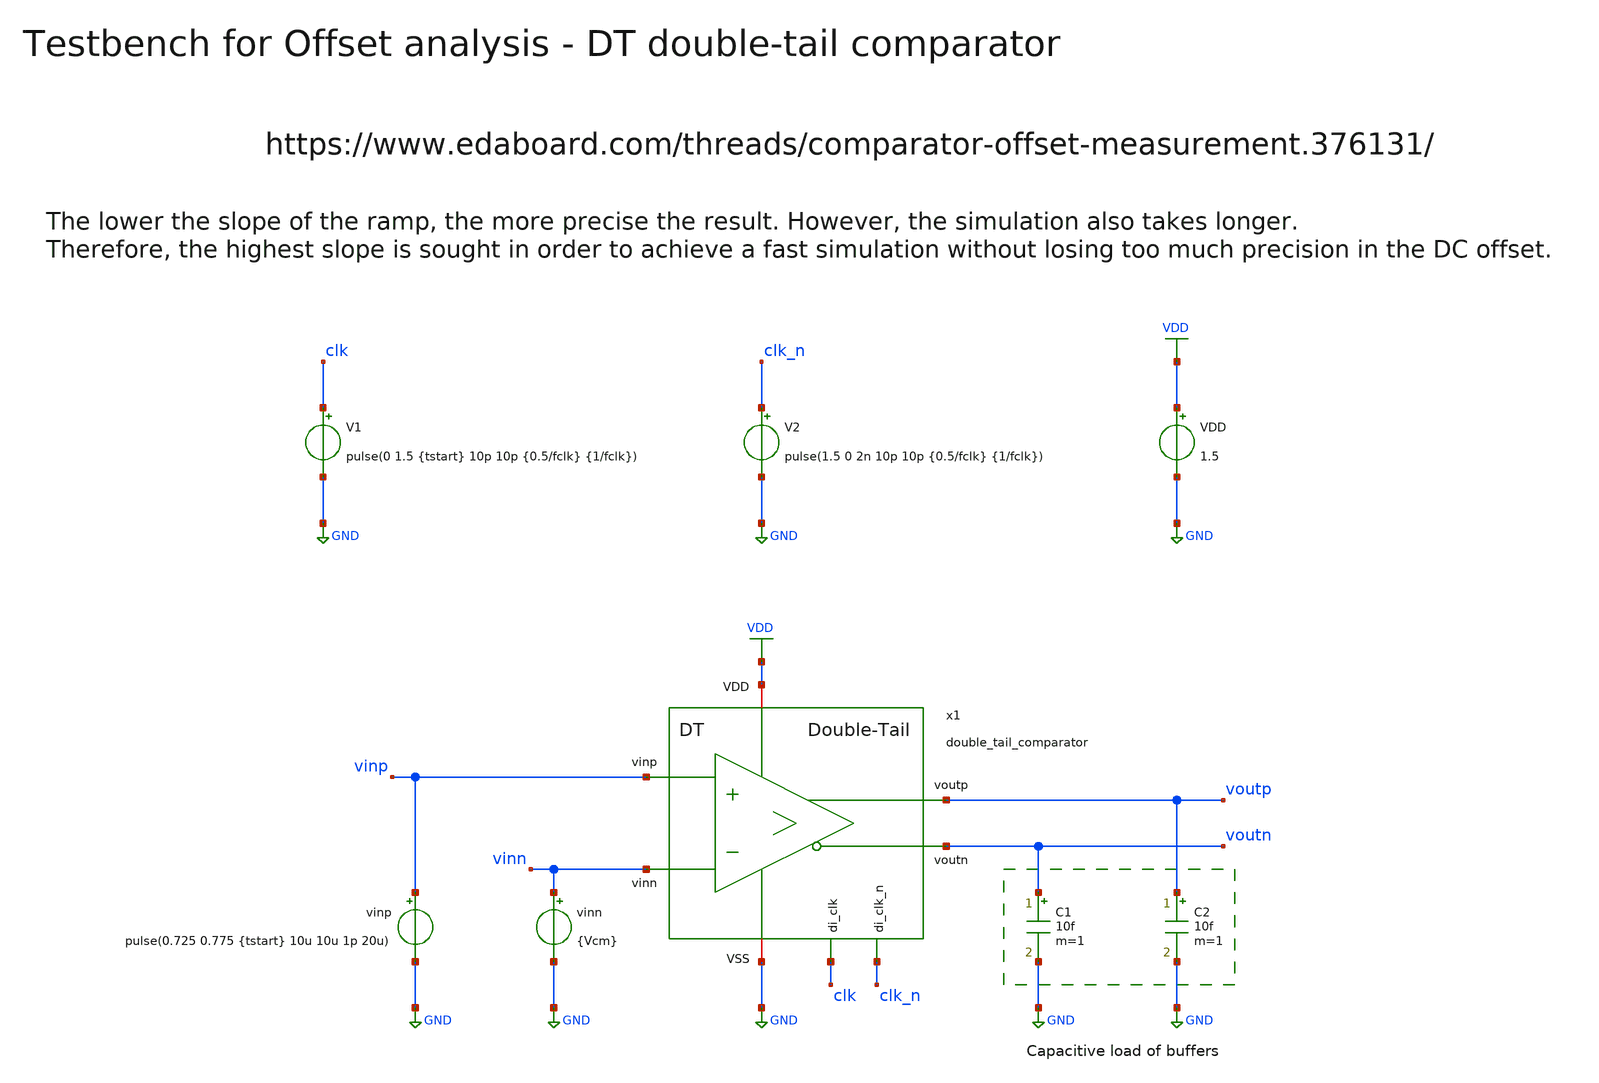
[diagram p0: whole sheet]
** sch_path: SG13G2_ATBS-ADC-main/xschem/comparator/discrete_time/Double-tail/testbenches/double_tail_comparator_tb_tran_offset.sch
**.subckt double_tail_comparator_tb_tran_offset
VDD VDD GND 1.5
V1 clk GND pulse(0 1.5 {tstart} 10p 10p {0.5/fclk} {1/fclk})
vinn vinn GND {Vcm}
vinp vinp GND pulse(0.725 0.775 {tstart} 10u 10u 1p 20u)
V2 clk_n GND pulse(1.5 0 2n 10p 10p {0.5/fclk} {1/fclk})
C1 voutn GND 10f m=1
C2 voutp GND 10f m=1
x1 clk_n clk VDD voutp vinp GND voutn vinn double_tail_comparator
**** begin user architecture code

.lib cornerMOSlv.lib mos_tt
.lib cornerMOShv.lib mos_tt
.lib cornerRES.lib res_typ



.param temp=27
.param fclk=8000000
.param tstart=2n
.param Vcm=0.75
.csparam fclk=fclk
.csparam tstart=tstart
.csparam Vcm=Vcm
.options klu method=gear reltol=1e-4 abstol=1e-12 gmin=1e-15
.control
* save all

* User Constants
let tstop = 20u
let tstep = 1/fclk

* Operating Point Analysis
op
remzerovec
write double_tail_comparator_tb_tran_offset.raw
set appendwrite

* Transient Analysis
tran $&tstep $&tstop
write double_tail_comparator_tb_tran_offset.raw

* Measure offset increasing ramp
let voutp_limit = 0.9 * 1.5
meas tran tcross WHEN v(voutp)=voutp_limit RISE=1
print tcross
meas tran vinp_voff FIND v(vinp) at=tcross
let voff_inc = vinp_voff - Vcm
print voff_inc

* Measure offset decreasing ramp
let voutn_limit = 0.9 * 1.5
let tmiddle = tstop/2
meas tran tcross WHEN v(voutn)=voutn_limit from=tmiddle RISE=1
print tcross
meas tran vinp_voff FIND v(vinp) at=tcross
let voff_dec = vinp_voff - Vcm
print voff_dec

* Plotting
plot v(clk) v(voutp) v(voutn) v(vinp) v(vinn)

*quit
.endc

**** end user architecture code
**.ends

* expanding   symbol:  comparator/discrete_time/Double-tail/double_tail_comparator.sym # of pins=8
** sym_path: SG13G2_ATBS-ADC-main/xschem/comparator/discrete_time/Double-tail/double_tail_comparator.sym
** sch_path: SG13G2_ATBS-ADC-main/xschem/comparator/discrete_time/Double-tail/double_tail_comparator.sch
.subckt double_tail_comparator di_clk_n di_clk VDD voutp vinp VSS voutn vinn
*.opin voutp
*.opin voutn
*.ipin di_clk_n
*.iopin VDD
*.iopin VSS
*.ipin vinp
*.ipin vinn
*.ipin di_clk
XM6 voutp vcpn VSS VSS sg13_lv_nmos w=1.0u l=0.13u ng=1 m=1 mm_ok=1
XM8 net1 di_clk_n VDD VDD sg13_lv_pmos w=2.0u l=0.13u ng=2 m=1 mm_ok=1
XM9 voutp voutn net1 VDD sg13_lv_pmos w=2.0u l=0.13u ng=2 m=1 mm_ok=1
XM10 voutn voutp net1 VDD sg13_lv_pmos w=2.0u l=0.13u ng=2 m=1 mm_ok=1
XM11 voutp voutn VSS VSS sg13_lv_nmos w=1.0u l=0.13u ng=1 m=1 mm_ok=1
XM12 voutn voutp VSS VSS sg13_lv_nmos w=1.0u l=0.13u ng=1 m=1 mm_ok=1
XM7 voutn vcpp VSS VSS sg13_lv_nmos w=1.0u l=0.13u ng=1 m=1 mm_ok=1
CP1 vcpn VSS 300f m=1
CP2 vcpp VSS 300f m=1
XM1 vcpn vinp vs VSS sg13_lv_nmos w=1.0u l=0.13u ng=1 m=1 mm_ok=1
XM2 vcpp vinn vs VSS sg13_lv_nmos w=1.0u l=0.13u ng=1 m=1 mm_ok=1
XM3 vs di_clk VSS VSS sg13_lv_nmos w=1.0u l=0.13u ng=1 m=1 mm_ok=1
XM4 vcpn di_clk VDD VDD sg13_lv_pmos w=1.0u l=0.13u ng=1 m=1 mm_ok=1
XM5 vcpp di_clk VDD VDD sg13_lv_pmos w=1.0u l=0.13u ng=1 m=1 mm_ok=1
.ends

.GLOBAL GND
.GLOBAL VDD
.end
